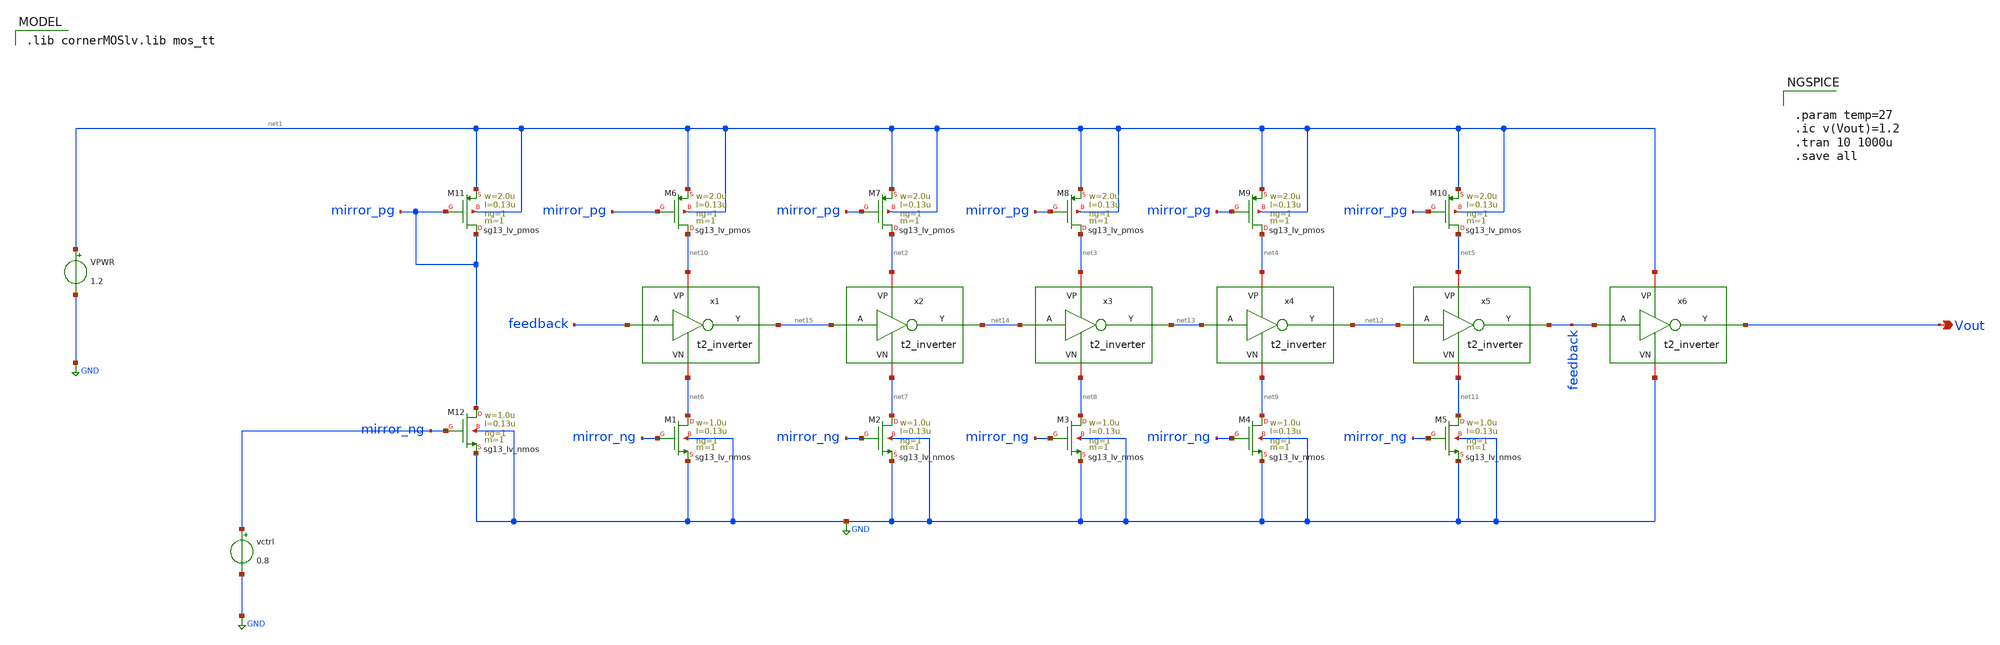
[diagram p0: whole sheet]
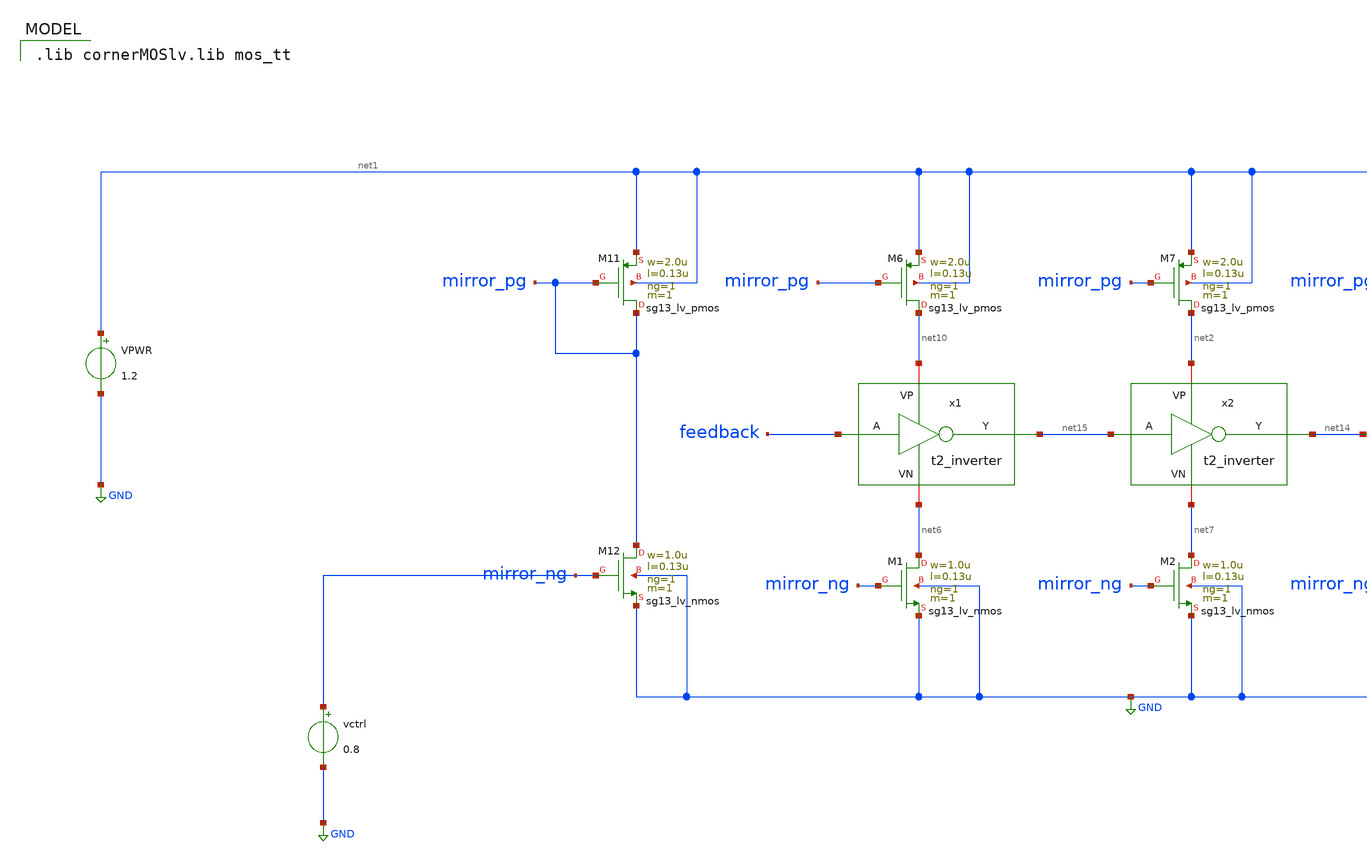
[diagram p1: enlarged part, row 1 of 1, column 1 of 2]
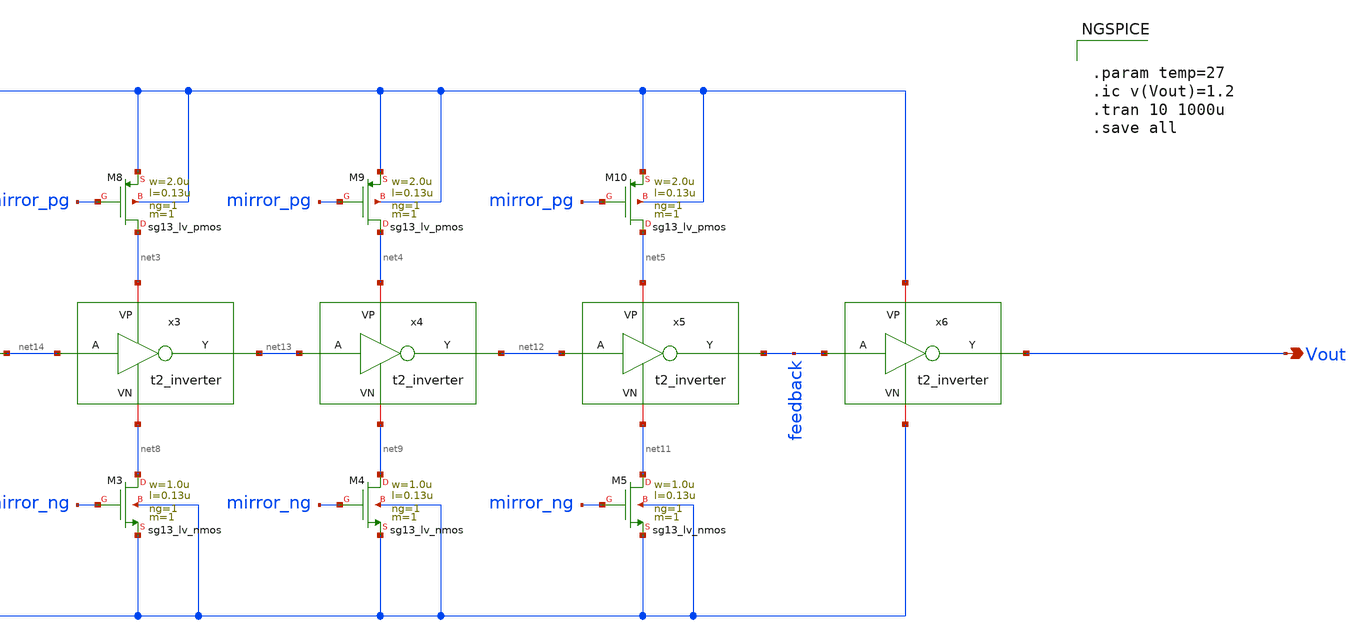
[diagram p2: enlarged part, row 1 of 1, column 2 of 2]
** sch_path: Team 2 Design/design_data/xschem/t2_vco_new_tb_.sch
**.subckt t2_vco_new_tb_ Vout
*.opin Vout
VPWR net1 GND 1.2
vctrl mirror_ng GND 0.8
x1 net10 feedback net15 net6 t2_inverter
x2 net2 net15 net14 net7 t2_inverter
x3 net3 net14 net13 net8 t2_inverter
x4 net4 net13 net12 net9 t2_inverter
x5 net5 net12 feedback net11 t2_inverter
XM1 net6 mirror_ng GND GND sg13_lv_nmos w=1.0u l=0.13u ng=1 m=1 mm_ok=1
XM2 net7 mirror_ng GND GND sg13_lv_nmos w=1.0u l=0.13u ng=1 m=1 mm_ok=1
XM3 net8 mirror_ng GND GND sg13_lv_nmos w=1.0u l=0.13u ng=1 m=1 mm_ok=1
XM4 net9 mirror_ng GND GND sg13_lv_nmos w=1.0u l=0.13u ng=1 m=1 mm_ok=1
XM5 net11 mirror_ng GND GND sg13_lv_nmos w=1.0u l=0.13u ng=1 m=1 mm_ok=1
XM6 net10 mirror_pg net1 net1 sg13_lv_pmos w=2.0u l=0.13u ng=1 m=1 mm_ok=1
XM7 net2 mirror_pg net1 net1 sg13_lv_pmos w=2.0u l=0.13u ng=1 m=1 mm_ok=1
XM8 net3 mirror_pg net1 net1 sg13_lv_pmos w=2.0u l=0.13u ng=1 m=1 mm_ok=1
XM9 net4 mirror_pg net1 net1 sg13_lv_pmos w=2.0u l=0.13u ng=1 m=1 mm_ok=1
XM10 net5 mirror_pg net1 net1 sg13_lv_pmos w=2.0u l=0.13u ng=1 m=1 mm_ok=1
XM11 mirror_pg mirror_pg net1 net1 sg13_lv_pmos w=2.0u l=0.13u ng=1 m=1 mm_ok=1
XM12 mirror_pg mirror_ng GND GND sg13_lv_nmos w=1.0u l=0.13u ng=1 m=1 mm_ok=1
x6 net1 feedback Vout GND t2_inverter
**** begin user architecture code
 .lib cornerMOSlv.lib mos_tt



.param temp=27
.ic v(Vout)=1.2
.tran 10 1000u
.save all


**** end user architecture code
**.ends

* expanding   symbol:  /foss/designs/cmos-pll-ihp-sg13g2/Team 2
*+ Design/design_data/xschem/t2_inverter.sym # of pins=4
** sym_path: Team 2 Design/design_data/xschem/t2_inverter.sym
** sch_path: Team 2 Design/design_data/xschem/t2_inverter.sch
.subckt t2_inverter VP A Y VN
*.iopin VP
*.iopin VN
*.ipin A
*.opin Y
XM2 Y A VP VP sg13_lv_pmos w=0.3u l=0.13u ng=1 m=1 mm_ok=1
XM1 Y A VN VN sg13_lv_nmos w=0.15u l=0.13u ng=1 m=1 mm_ok=1
.ends

.GLOBAL GND
.end
